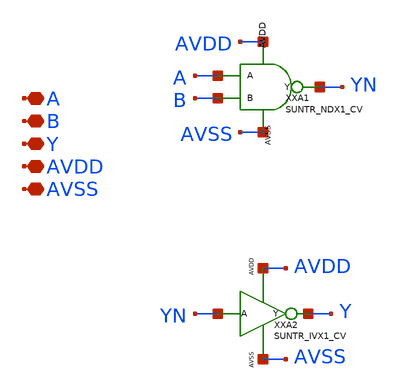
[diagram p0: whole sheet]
** sch_path: ip/sun_tr_sky130nm/design/SUN_TR_SKY130NM/SUNTR_ANX2_CV.sch
**.subckt SUNTR_ANX2_CV A B Y AVDD AVSS
*.iopin A
*.iopin B
*.iopin Y
*.iopin AVDD
*.iopin AVSS
XXA1 A B YN AVDD AVSS SUNTR_NDX1_CV
XXA2 YN Y AVDD AVSS SUNTR_IVX1_CV
**.ends
.end
